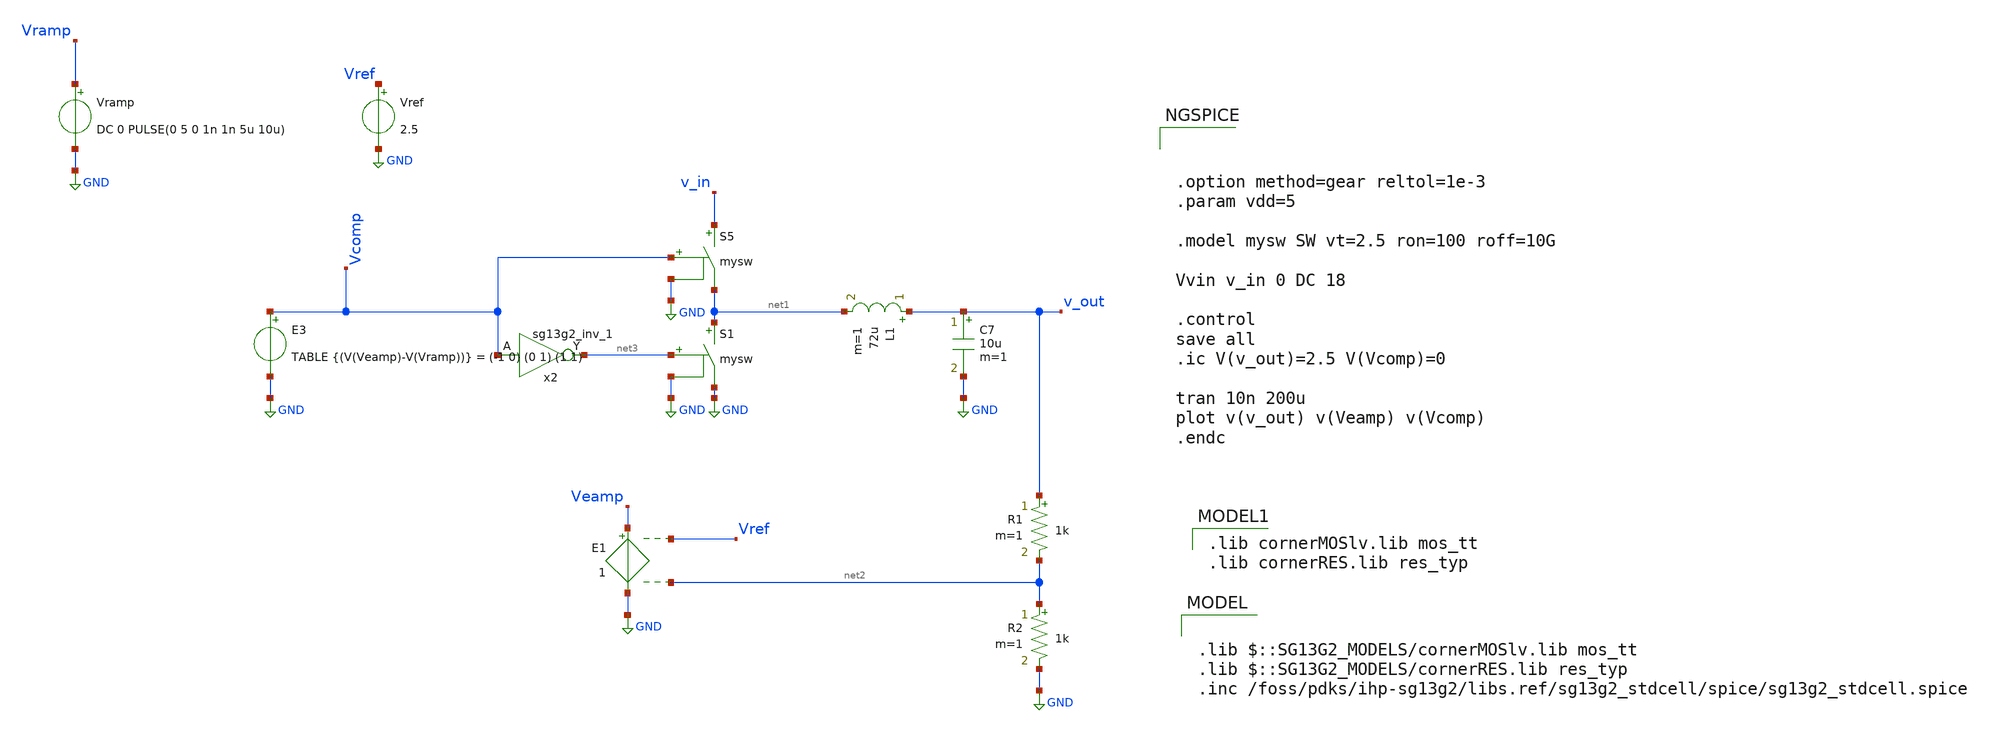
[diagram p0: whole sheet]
** sch_path: Designs/ideal_circuits/ideal_dcdc.sch
* (c) 2025 Thesis_HP, Apache-2.0 license
**.subckt ideal_dcdc
Vramp Vramp GND DC 0 PULSE(0 5 0 1n 1n 5u 10u)
S5 v_in net1 Vcomp GND mysw
S1 net1 GND net3 GND mysw
L1 v_out net1 72u m=1
C7 v_out GND 10u m=1
R1 v_out net2 1k m=1
R2 net2 GND 1k m=1
Vref Vref GND 2.5
E1 Veamp GND Vref net2 1
x2 net3 Vcomp 1.5 0 sg13g2_inv_1
E3 Vcomp GND TABLE {(V(Veamp)-V(Vramp))} = (-1 0) (0 1) (1 1)
**** begin user architecture code



.option method=gear reltol=1e-3
.param vdd=5

.model mysw SW vt=2.5 ron=100 roff=10G

Vvin v_in 0 DC 18

.control
save all
.ic V(v_out)=2.5 V(Vcomp)=0

tran 10n 200u
plot v(v_out) v(Veamp) v(Vcomp)
.endc


 .lib cornerMOSlv.lib mos_tt
.lib cornerRES.lib res_typ


.lib $::SG13G2_MODELS/cornerMOSlv.lib mos_tt
.lib $::SG13G2_MODELS/cornerRES.lib res_typ
.inc /foss/pdks/ihp-sg13g2/libs.ref/sg13g2_stdcell/spice/sg13g2_stdcell.spice

**** end user architecture code
**.ends

* expanding   symbol:  sg13g2_stdcells/sg13g2_inv_1.sym # of pins=2
** sym_path: sg13g2_stdcells/sg13g2_inv_1.sym
** sch_path: sg13g2_stdcells/sg13g2_inv_1.sch
.subckt sg13g2_inv_1 Y A VDD VSS
*.opin Y
*.ipin A
*.iopin VDD
*.iopin VSS
XM1 Y A VSS VSS sg13_lv_nmos w=740.00n l=130.00n ng=1 m=1 mm_ok=1
XM2 Y A VDD VDD sg13_lv_pmos w=1.12u l=130.00n ng=1 m=1 mm_ok=1
.ends

.GLOBAL GND
.end
